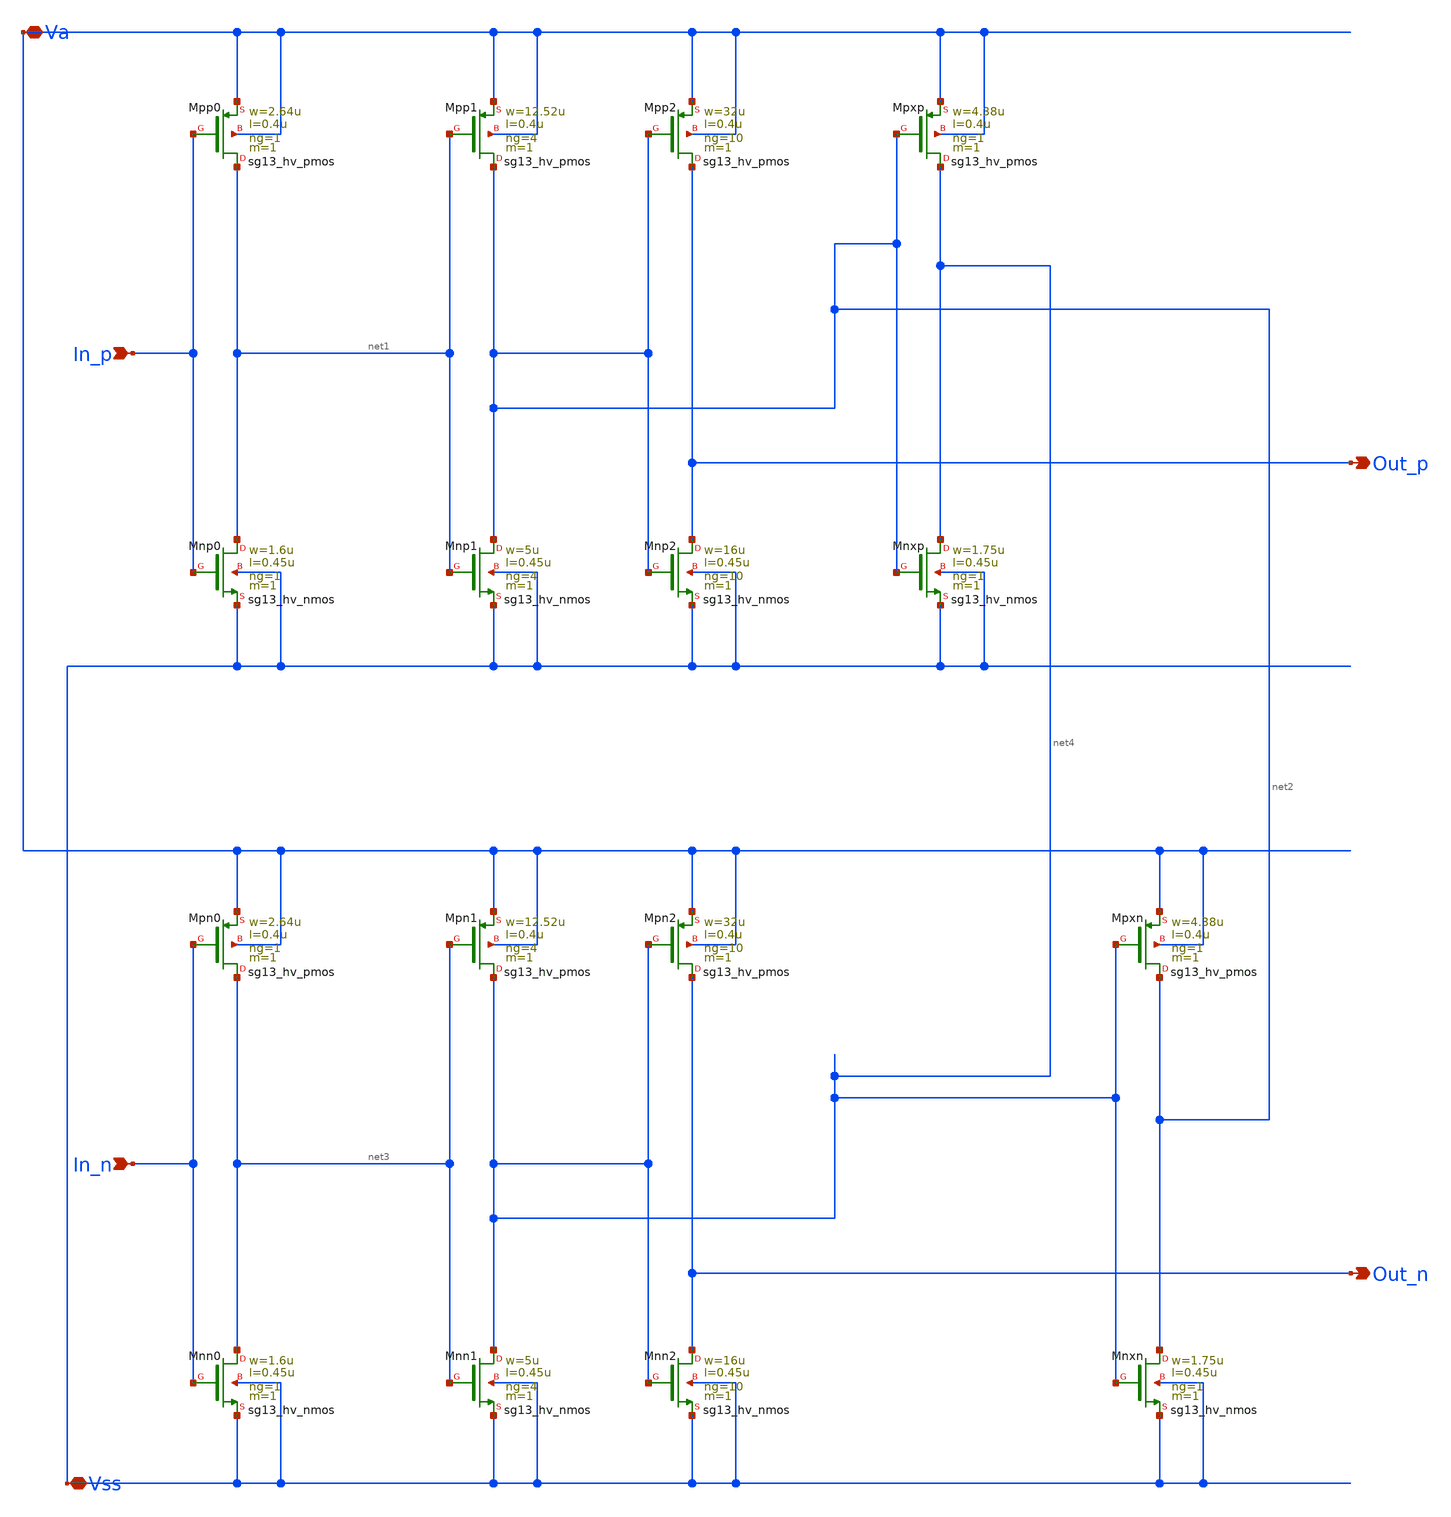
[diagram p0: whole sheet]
** sch_path: macros/lvds_tx/schematic/xschem/predriver_stage.sch
**.subckt predriver_stage In_p Out_p In_n Out_n Va Vss
*.ipin In_p
*.opin Out_p
*.ipin In_n
*.opin Out_n
*.iopin Va
*.iopin Vss
XMpp0 net1 In_p Va Va sg13_hv_pmos w=2.64u l=0.4u ng=1 m=1 mm_ok=1
XMnp0 net1 In_p Vss Vss sg13_hv_nmos w=1.6u l=0.45u ng=1 m=1 mm_ok=1
XMpp1 net2 net1 Va Va sg13_hv_pmos w=12.52u l=0.4u ng=4 m=1 mm_ok=1
XMnp1 net2 net1 Vss Vss sg13_hv_nmos w=5u l=0.45u ng=4 m=1 mm_ok=1
XMpp2 Out_p net2 Va Va sg13_hv_pmos w=32u l=0.4u ng=10 m=1 mm_ok=1
XMnp2 Out_p net2 Vss Vss sg13_hv_nmos w=16u l=0.45u ng=10 m=1 mm_ok=1
XMpn0 net3 In_n Va Va sg13_hv_pmos w=2.64u l=0.4u ng=1 m=1 mm_ok=1
XMnn0 net3 In_n Vss Vss sg13_hv_nmos w=1.6u l=0.45u ng=1 m=1 mm_ok=1
XMpn1 net4 net3 Va Va sg13_hv_pmos w=12.52u l=0.4u ng=4 m=1 mm_ok=1
XMnn1 net4 net3 Vss Vss sg13_hv_nmos w=5u l=0.45u ng=4 m=1 mm_ok=1
XMpn2 Out_n net4 Va Va sg13_hv_pmos w=32u l=0.4u ng=10 m=1 mm_ok=1
XMnn2 Out_n net4 Vss Vss sg13_hv_nmos w=16u l=0.45u ng=10 m=1 mm_ok=1
XMpxp net4 net2 Va Va sg13_hv_pmos w=4.38u l=0.4u ng=1 m=1 mm_ok=1
XMnxp net4 net2 Vss Vss sg13_hv_nmos w=1.75u l=0.45u ng=1 m=1 mm_ok=1
XMpxn net2 net4 Va Va sg13_hv_pmos w=4.38u l=0.4u ng=1 m=1 mm_ok=1
XMnxn net2 net4 Vss Vss sg13_hv_nmos w=1.75u l=0.45u ng=1 m=1 mm_ok=1
**.ends
.end
